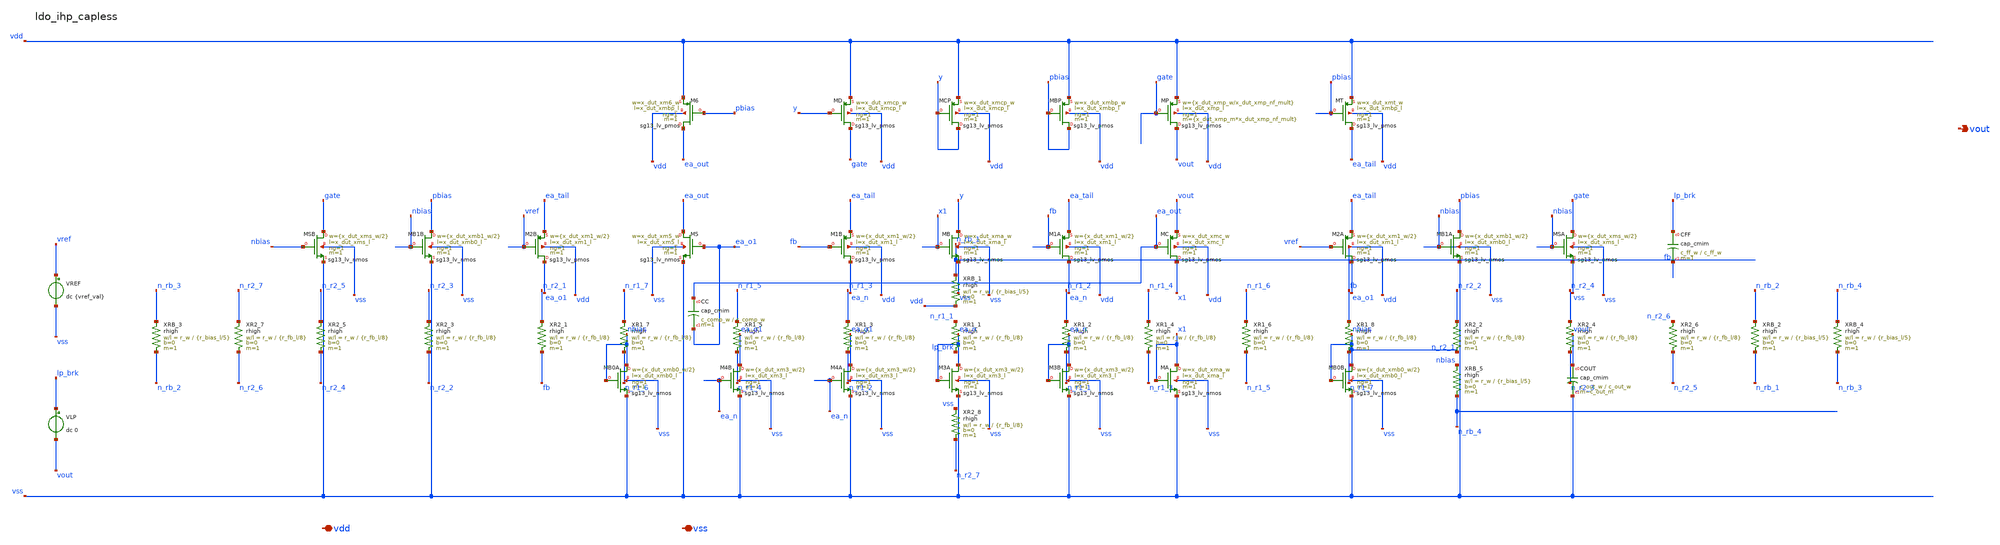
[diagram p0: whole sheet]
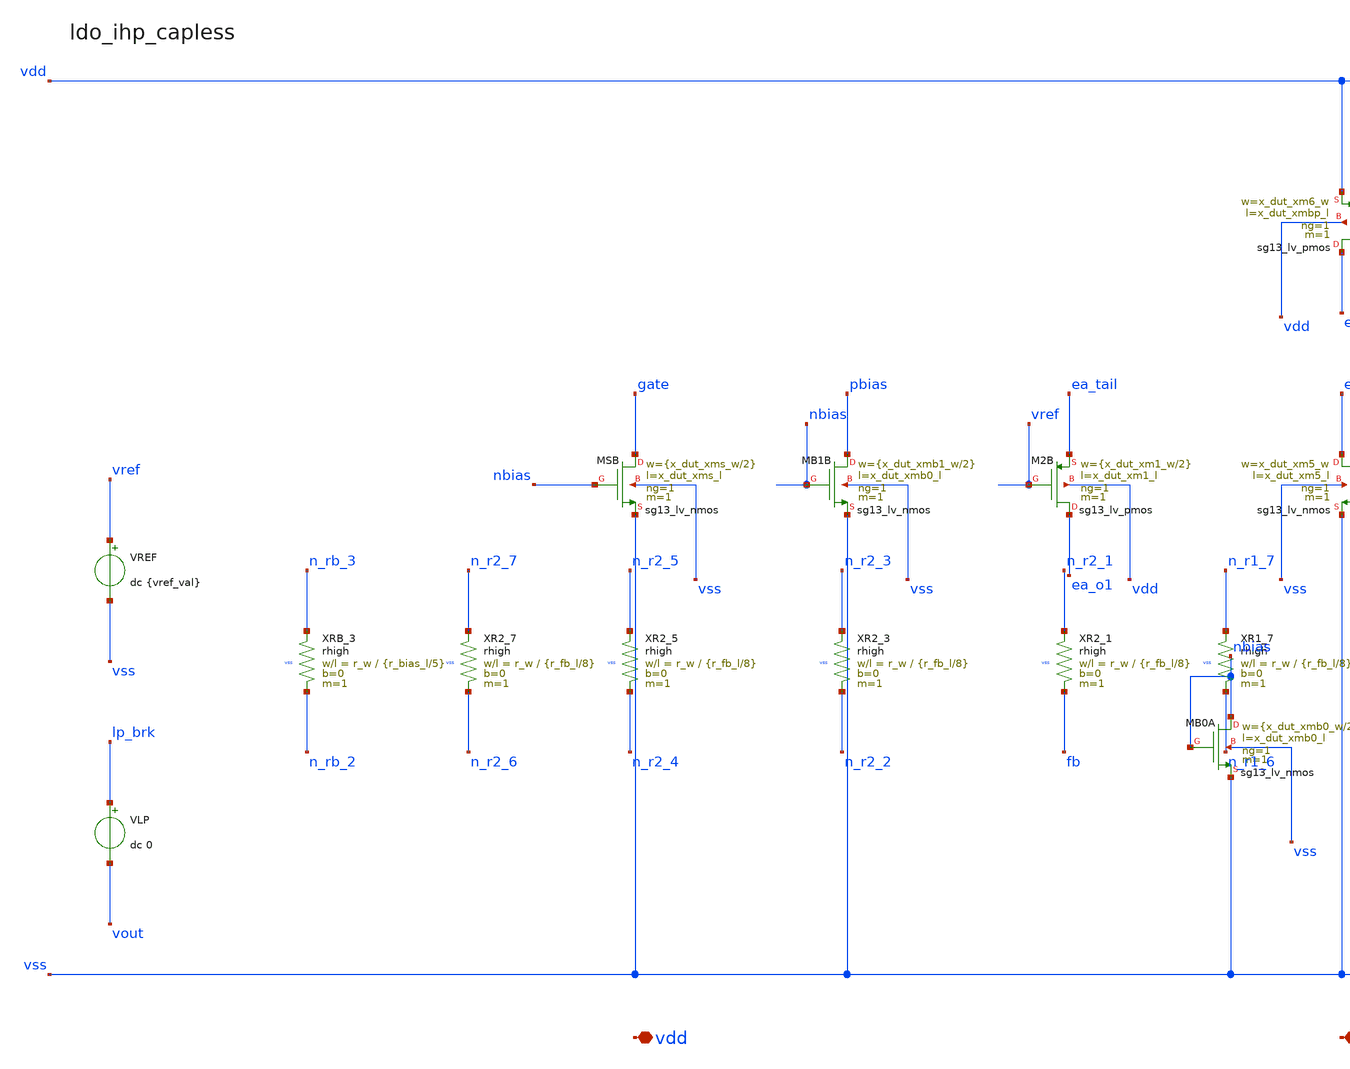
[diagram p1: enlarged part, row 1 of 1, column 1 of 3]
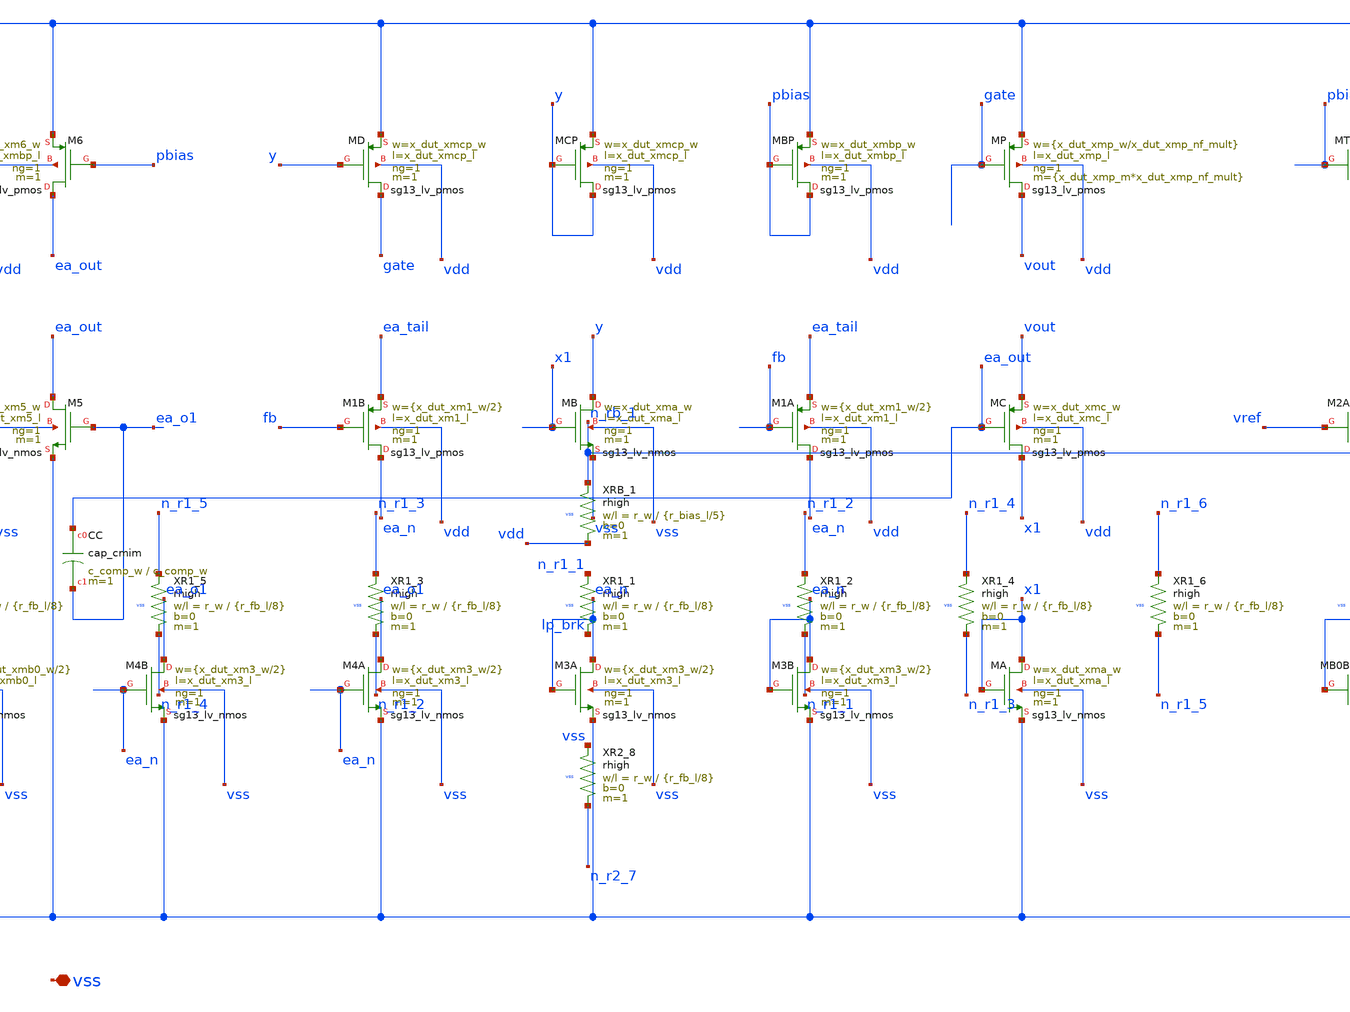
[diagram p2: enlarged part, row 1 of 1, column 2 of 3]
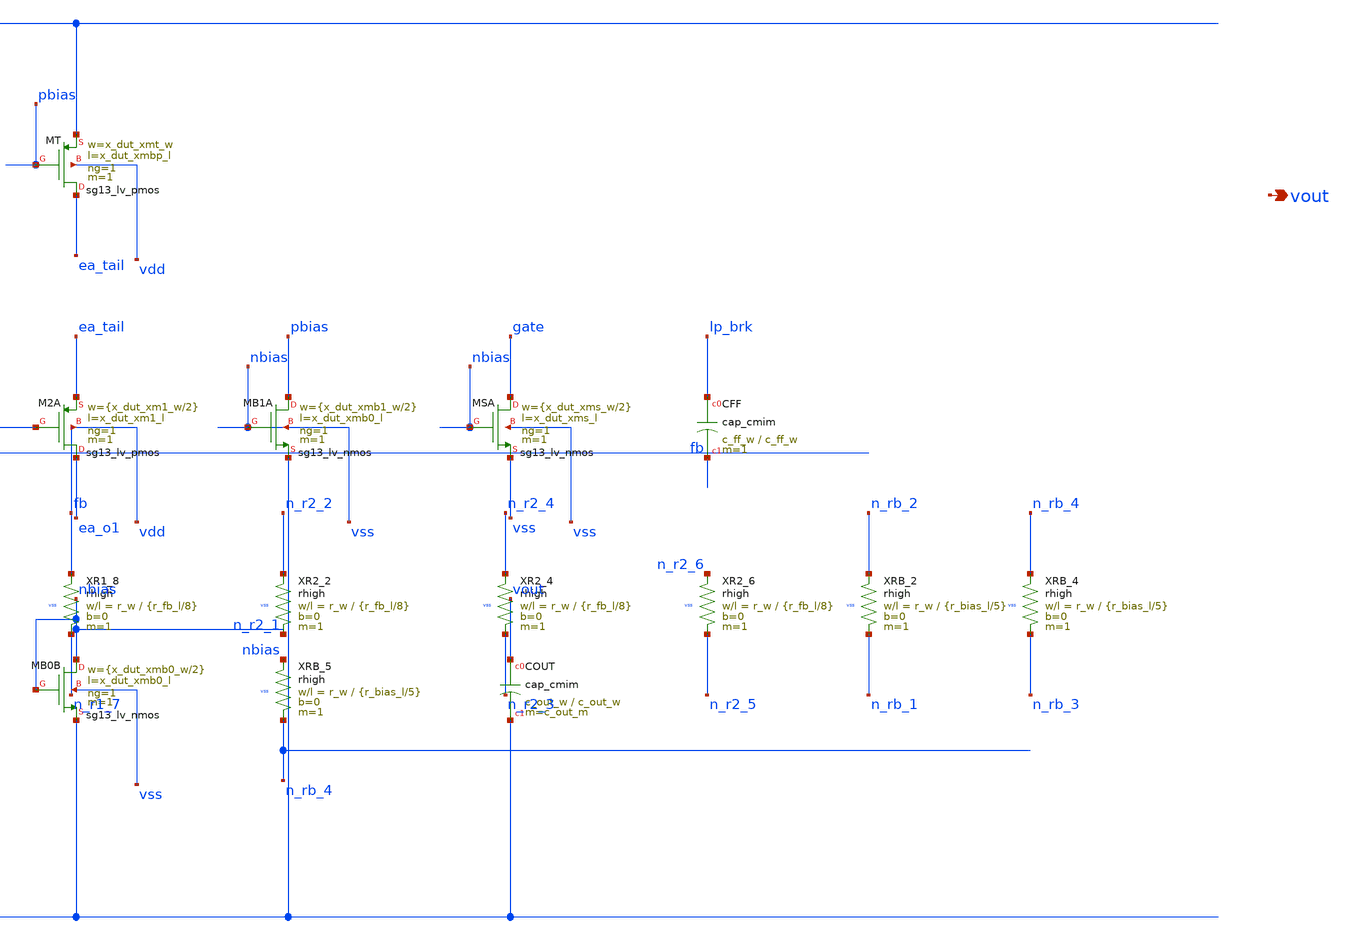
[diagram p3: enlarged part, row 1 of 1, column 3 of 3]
** sch_path: analog-db/circuits/ldo_010_capless_lowiq/pdk/ihp-sg13g2/schematic/ldo_ihp_capless_flat.sch
**.subckt ldo_ihp_capless_flat vdd vss vout
*.iopin vdd
*.iopin vss
*.opin vout
VREF vref vss dc {vref_val}
VLP lp_brk vout dc 0
XR1_1 lp_brk n_r1_1 vss rhigh w=r_w l={r_fb_l/8} m=1 b=0
XR1_2 n_r1_1 n_r1_2 vss rhigh w=r_w l={r_fb_l/8} m=1 b=0
XR1_3 n_r1_2 n_r1_3 vss rhigh w=r_w l={r_fb_l/8} m=1 b=0
XR1_4 n_r1_3 n_r1_4 vss rhigh w=r_w l={r_fb_l/8} m=1 b=0
XR1_5 n_r1_4 n_r1_5 vss rhigh w=r_w l={r_fb_l/8} m=1 b=0
XR1_6 n_r1_5 n_r1_6 vss rhigh w=r_w l={r_fb_l/8} m=1 b=0
XR1_7 n_r1_6 n_r1_7 vss rhigh w=r_w l={r_fb_l/8} m=1 b=0
XR1_8 n_r1_7 fb vss rhigh w=r_w l={r_fb_l/8} m=1 b=0
XCFF lp_brk fb cap_cmim w=c_ff_w l=c_ff_w m=1
XR2_1 fb n_r2_1 vss rhigh w=r_w l={r_fb_l/8} m=1 b=0
XR2_2 n_r2_1 n_r2_2 vss rhigh w=r_w l={r_fb_l/8} m=1 b=0
XR2_3 n_r2_2 n_r2_3 vss rhigh w=r_w l={r_fb_l/8} m=1 b=0
XR2_4 n_r2_3 n_r2_4 vss rhigh w=r_w l={r_fb_l/8} m=1 b=0
XR2_5 n_r2_4 n_r2_5 vss rhigh w=r_w l={r_fb_l/8} m=1 b=0
XR2_6 n_r2_5 n_r2_6 vss rhigh w=r_w l={r_fb_l/8} m=1 b=0
XR2_7 n_r2_6 n_r2_7 vss rhigh w=r_w l={r_fb_l/8} m=1 b=0
XR2_8 n_r2_7 vss vss rhigh w=r_w l={r_fb_l/8} m=1 b=0
XRB_1 vdd n_rb_1 vss rhigh w=r_w l={r_bias_l/5} m=1 b=0
XRB_2 n_rb_1 n_rb_2 vss rhigh w=r_w l={r_bias_l/5} m=1 b=0
XRB_3 n_rb_2 n_rb_3 vss rhigh w=r_w l={r_bias_l/5} m=1 b=0
XRB_4 n_rb_3 n_rb_4 vss rhigh w=r_w l={r_bias_l/5} m=1 b=0
XRB_5 n_rb_4 nbias vss rhigh w=r_w l={r_bias_l/5} m=1 b=0
XMB0A nbias nbias vss vss sg13_lv_nmos w={x_dut_xmb0_w/2} l=x_dut_xmb0_l ng=1 m=1 mm_ok=1
XMB0B nbias nbias vss vss sg13_lv_nmos w={x_dut_xmb0_w/2} l=x_dut_xmb0_l ng=1 m=1 mm_ok=1
XMB1A pbias nbias vss vss sg13_lv_nmos w={x_dut_xmb1_w/2} l=x_dut_xmb0_l ng=1 m=1 mm_ok=1
XMB1B pbias nbias vss vss sg13_lv_nmos w={x_dut_xmb1_w/2} l=x_dut_xmb0_l ng=1 m=1 mm_ok=1
XMBP pbias pbias vdd vdd sg13_lv_pmos w=x_dut_xmbp_w l=x_dut_xmbp_l ng=1 m=1 mm_ok=1
XMT ea_tail pbias vdd vdd sg13_lv_pmos w=x_dut_xmt_w l=x_dut_xmbp_l ng=1 m=1 mm_ok=1
XM1A ea_n fb ea_tail vdd sg13_lv_pmos w={x_dut_xm1_w/2} l=x_dut_xm1_l ng=1 m=1 mm_ok=1
XM1B ea_n fb ea_tail vdd sg13_lv_pmos w={x_dut_xm1_w/2} l=x_dut_xm1_l ng=1 m=1 mm_ok=1
XM2A ea_o1 vref ea_tail vdd sg13_lv_pmos w={x_dut_xm1_w/2} l=x_dut_xm1_l ng=1 m=1 mm_ok=1
XM2B ea_o1 vref ea_tail vdd sg13_lv_pmos w={x_dut_xm1_w/2} l=x_dut_xm1_l ng=1 m=1 mm_ok=1
XM3A ea_n ea_n vss vss sg13_lv_nmos w={x_dut_xm3_w/2} l=x_dut_xm3_l ng=1 m=1 mm_ok=1
XM3B ea_n ea_n vss vss sg13_lv_nmos w={x_dut_xm3_w/2} l=x_dut_xm3_l ng=1 m=1 mm_ok=1
XM4A ea_o1 ea_n vss vss sg13_lv_nmos w={x_dut_xm3_w/2} l=x_dut_xm3_l ng=1 m=1 mm_ok=1
XM4B ea_o1 ea_n vss vss sg13_lv_nmos w={x_dut_xm3_w/2} l=x_dut_xm3_l ng=1 m=1 mm_ok=1
XM5 ea_out ea_o1 vss vss sg13_lv_nmos w=x_dut_xm5_w l=x_dut_xm5_l ng=1 m=1 mm_ok=1
XM6 ea_out pbias vdd vdd sg13_lv_pmos w=x_dut_xm6_w l=x_dut_xmbp_l ng=1 m=1 mm_ok=1
XCC ea_out ea_o1 cap_cmim w=c_comp_w l=c_comp_w m=1
XMC x1 ea_out vout vdd sg13_lv_pmos w=x_dut_xmc_w l=x_dut_xmc_l ng=1 m=1 mm_ok=1
XMA x1 x1 vss vss sg13_lv_nmos w=x_dut_xma_w l=x_dut_xma_l ng=1 m=1 mm_ok=1
XMB y x1 vss vss sg13_lv_nmos w=x_dut_xma_w l=x_dut_xma_l ng=1 m=1 mm_ok=1
XMCP y y vdd vdd sg13_lv_pmos w=x_dut_xmcp_w l=x_dut_xmcp_l ng=1 m=1 mm_ok=1
XMD gate y vdd vdd sg13_lv_pmos w=x_dut_xmcp_w l=x_dut_xmcp_l ng=1 m=1 mm_ok=1
XMSA gate nbias vss vss sg13_lv_nmos w={x_dut_xms_w/2} l=x_dut_xms_l ng=1 m=1 mm_ok=1
XMSB gate nbias vss vss sg13_lv_nmos w={x_dut_xms_w/2} l=x_dut_xms_l ng=1 m=1 mm_ok=1
XMP vout gate vdd vdd sg13_lv_pmos w={x_dut_xmp_w/x_dut_xmp_nf_mult} l=x_dut_xmp_l ng=1 m={x_dut_xmp_m*x_dut_xmp_nf_mult}
+ mm_ok=1
XCOUT vout vss cap_cmim w=c_out_w l=c_out_w m=c_out_m
**.ends
.end
